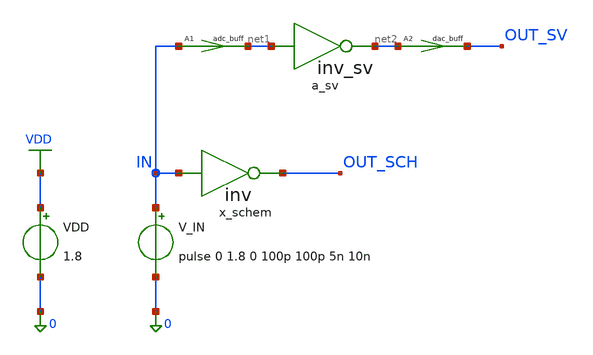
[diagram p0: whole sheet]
** sch_path: designs_backup/designs/inv_mixed/inv_test_1.sch
**.subckt inv_test_1
x_schem IN OUT_SCH inv
V_IN IN 0 pulse 0 1.8 0 100p 100p 5n 10n
VDD VDD 0 1.8
Aa_sv [ net1 ] [ net2 ] inv_sv
A1 [ IN ] [ net1 ] adc_buff
A2 [ net2 ] [ OUT_SV ] dac_buff
**** begin user architecture code

** opencircuitdesign pdks install
.lib $::SKYWATER_MODELS/sky130.lib.spice tt



.control
  save all
  tran 10p 30n
  write inv_test_1.raw
  write /foss/designs/inv_mixed/inv_test_1.raw
  quit
.endc


**** end user architecture code
**.ends

* expanding   symbol:  inv.sym # of pins=2
** sym_path: designs_backup/designs/inv_mixed/xschem/inv.sym
** sch_path: designs_backup/designs/inv_mixed/xschem/inv.sch
.subckt inv IN OUT
*.opin OUT
*.ipin IN
XM1 OUT IN VDD VDD sky130_fd_pr__pfet_01v8 L=0.15 W=0.42 nf=1 ad='int((1 + 1)/2) * 0.42 / 1 * 0.29' as='int((1 + 2)/2) * 0.42 / 1 * 0.29'
+ pd='2*int((1 + 1)/2) * (0.42 / 1 + 0.29)' ps='2*int((1 + 2)/2) * (0.42 / 1 + 0.29)' nrd='0.29 / 0.42 '
+ nrs='0.29 / 0.42 ' sa=0 sb=0 sd=0 mult=1 m=1
XM3 OUT IN 0 0 sky130_fd_pr__nfet_01v8 L=0.15 W=0.42 nf=1 ad='int((1 + 1)/2) * 0.42 / 1 * 0.29' as='int((1 + 2)/2) * 0.42 / 1 * 0.29'
+ pd='2*int((1 + 1)/2) * (0.42 / 1 + 0.29)' ps='2*int((1 + 2)/2) * (0.42 / 1 + 0.29)' nrd='0.29 / 0.42 '
+ nrs='0.29 / 0.42 ' sa=0 sb=0 sd=0 mult=1 m=1
.ends

.GLOBAL VDD
**** begin user architecture code
.model adc_buff adc_bridge(in_low=0.6 in_high=1.2 rise_delay=10n fall_delay=10n)
.model inv_sv d_cosim simulation="ivlng" sim_args=["inv_sv.vvp"]
.model dac_buff dac_bridge(input_load=1e-15 t_rise=10n t_fall=10n out_low=0 out_high=1.8)
**** end user architecture code
.end
